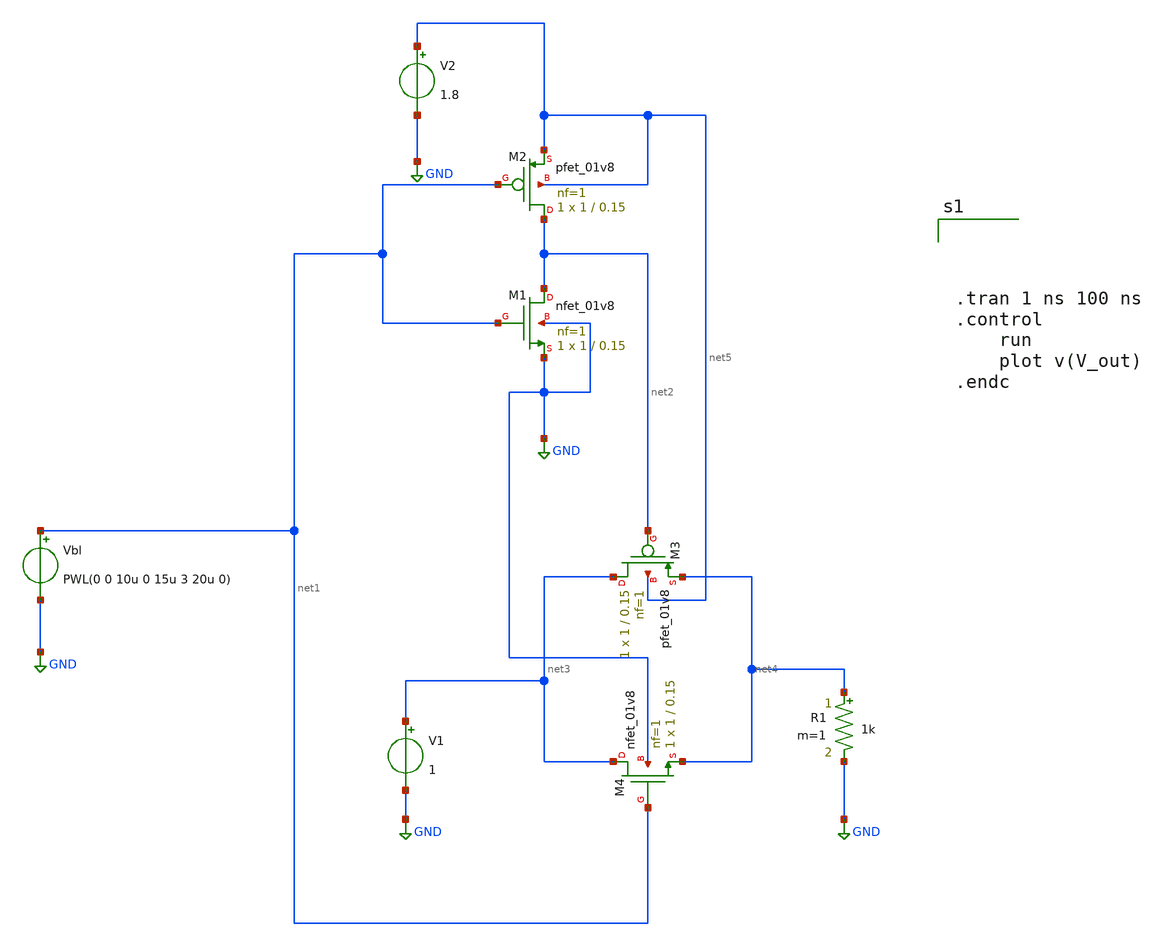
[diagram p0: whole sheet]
** sch_path: hopfield/switch_inv.sch
**.subckt switch_inv
XM1 net2 net1 GND GND sky130_fd_pr__nfet_01v8 L=0.15 W=1 nf=1 ad='int((nf+1)/2) * W/nf * 0.29' as='int((nf+2)/2) * W/nf * 0.29'
+ pd='2*int((nf+1)/2) * (W/nf + 0.29)' ps='2*int((nf+2)/2) * (W/nf + 0.29)' nrd='0.29 / W' nrs='0.29 / W'
+ sa=0 sb=0 sd=0 mult=1 m=1
XM2 net2 net1 net5 net5 sky130_fd_pr__pfet_01v8 L=0.15 W=1 nf=1 ad='int((nf+1)/2) * W/nf * 0.29' as='int((nf+2)/2) * W/nf * 0.29'
+ pd='2*int((nf+1)/2) * (W/nf + 0.29)' ps='2*int((nf+2)/2) * (W/nf + 0.29)' nrd='0.29 / W' nrs='0.29 / W'
+ sa=0 sb=0 sd=0 mult=1 m=1
XM3 net3 net2 net4 net5 sky130_fd_pr__pfet_01v8 L=0.15 W=1 nf=1 ad='int((nf+1)/2) * W/nf * 0.29' as='int((nf+2)/2) * W/nf * 0.29'
+ pd='2*int((nf+1)/2) * (W/nf + 0.29)' ps='2*int((nf+2)/2) * (W/nf + 0.29)' nrd='0.29 / W' nrs='0.29 / W'
+ sa=0 sb=0 sd=0 mult=1 m=1
XM4 net3 net1 net4 GND sky130_fd_pr__nfet_01v8 L=0.15 W=1 nf=1 ad='int((nf+1)/2) * W/nf * 0.29' as='int((nf+2)/2) * W/nf * 0.29'
+ pd='2*int((nf+1)/2) * (W/nf + 0.29)' ps='2*int((nf+2)/2) * (W/nf + 0.29)' nrd='0.29 / W' nrs='0.29 / W'
+ sa=0 sb=0 sd=0 mult=1 m=1
Vbl net1 GND PWL(0 0 10u 0 15u 3 20u 0)
V2 net5 GND 1.8
V1 net3 GND 1
R1 net4 GND 1k m=1
**** begin user architecture code




.tran 1 ns 100 ns
.control
	run
	plot v(V_out)
.endc


**** end user architecture code
**.ends
.GLOBAL GND
.end
